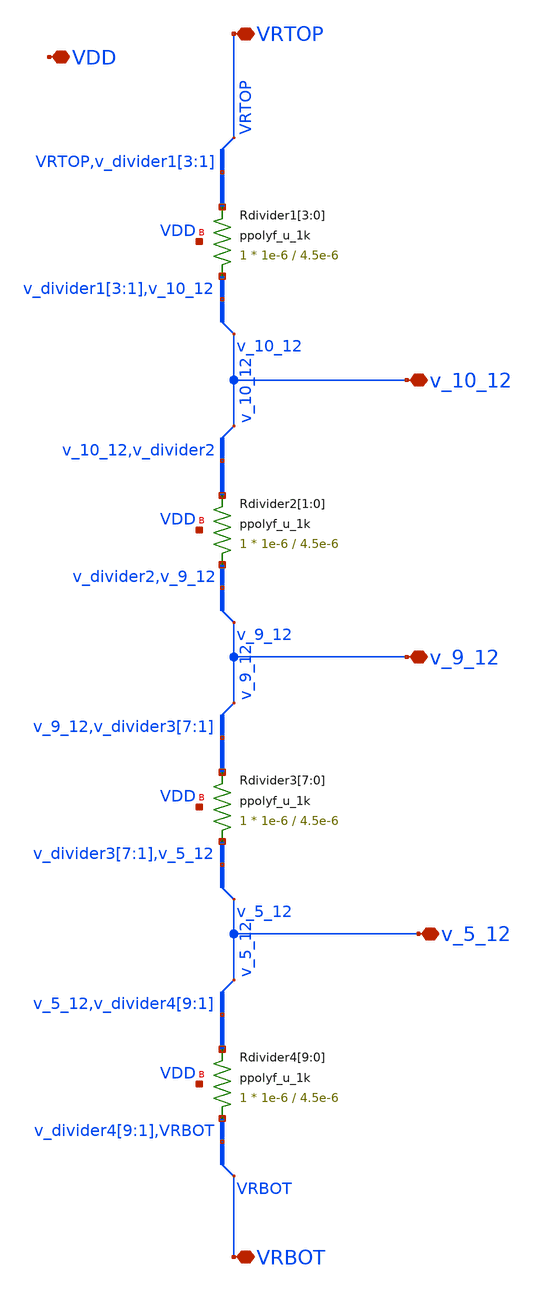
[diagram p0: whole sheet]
** sch_path: designs/libs/core_biasgen/biasgen_resistor_divider/biasgen_resistor_divider.sch
**.subckt biasgen_resistor_divider VRTOP VRBOT v_10_12 v_9_12 v_5_12 VDD
*.iopin VRTOP
*.iopin VRBOT
*.iopin v_10_12
*.iopin v_9_12
*.iopin v_5_12
*.iopin VDD
XRdivider1[3] v_divider1[3] VRTOP VDD ppolyf_u_1k r_width=1e-6 r_length=4.5e-6 m=1
XRdivider1[2] v_divider1[2] v_divider1[3] VDD ppolyf_u_1k r_width=1e-6 r_length=4.5e-6 m=1
XRdivider1[1] v_divider1[1] v_divider1[2] VDD ppolyf_u_1k r_width=1e-6 r_length=4.5e-6 m=1
XRdivider1[0] v_10_12 v_divider1[1] VDD ppolyf_u_1k r_width=1e-6 r_length=4.5e-6 m=1
XRdivider2[1] v_divider2 v_10_12 VDD ppolyf_u_1k r_width=1e-6 r_length=4.5e-6 m=1
XRdivider2[0] v_9_12 v_divider2 VDD ppolyf_u_1k r_width=1e-6 r_length=4.5e-6 m=1
XRdivider3[7] v_divider3[7] v_9_12 VDD ppolyf_u_1k r_width=1e-6 r_length=4.5e-6 m=1
XRdivider3[6] v_divider3[6] v_divider3[7] VDD ppolyf_u_1k r_width=1e-6 r_length=4.5e-6 m=1
XRdivider3[5] v_divider3[5] v_divider3[6] VDD ppolyf_u_1k r_width=1e-6 r_length=4.5e-6 m=1
XRdivider3[4] v_divider3[4] v_divider3[5] VDD ppolyf_u_1k r_width=1e-6 r_length=4.5e-6 m=1
XRdivider3[3] v_divider3[3] v_divider3[4] VDD ppolyf_u_1k r_width=1e-6 r_length=4.5e-6 m=1
XRdivider3[2] v_divider3[2] v_divider3[3] VDD ppolyf_u_1k r_width=1e-6 r_length=4.5e-6 m=1
XRdivider3[1] v_divider3[1] v_divider3[2] VDD ppolyf_u_1k r_width=1e-6 r_length=4.5e-6 m=1
XRdivider3[0] v_5_12 v_divider3[1] VDD ppolyf_u_1k r_width=1e-6 r_length=4.5e-6 m=1
XRdivider4[9] v_divider4[9] v_5_12 VDD ppolyf_u_1k r_width=1e-6 r_length=4.5e-6 m=1
XRdivider4[8] v_divider4[8] v_divider4[9] VDD ppolyf_u_1k r_width=1e-6 r_length=4.5e-6 m=1
XRdivider4[7] v_divider4[7] v_divider4[8] VDD ppolyf_u_1k r_width=1e-6 r_length=4.5e-6 m=1
XRdivider4[6] v_divider4[6] v_divider4[7] VDD ppolyf_u_1k r_width=1e-6 r_length=4.5e-6 m=1
XRdivider4[5] v_divider4[5] v_divider4[6] VDD ppolyf_u_1k r_width=1e-6 r_length=4.5e-6 m=1
XRdivider4[4] v_divider4[4] v_divider4[5] VDD ppolyf_u_1k r_width=1e-6 r_length=4.5e-6 m=1
XRdivider4[3] v_divider4[3] v_divider4[4] VDD ppolyf_u_1k r_width=1e-6 r_length=4.5e-6 m=1
XRdivider4[2] v_divider4[2] v_divider4[3] VDD ppolyf_u_1k r_width=1e-6 r_length=4.5e-6 m=1
XRdivider4[1] v_divider4[1] v_divider4[2] VDD ppolyf_u_1k r_width=1e-6 r_length=4.5e-6 m=1
XRdivider4[0] VRBOT v_divider4[1] VDD ppolyf_u_1k r_width=1e-6 r_length=4.5e-6 m=1
**.ends
.end
